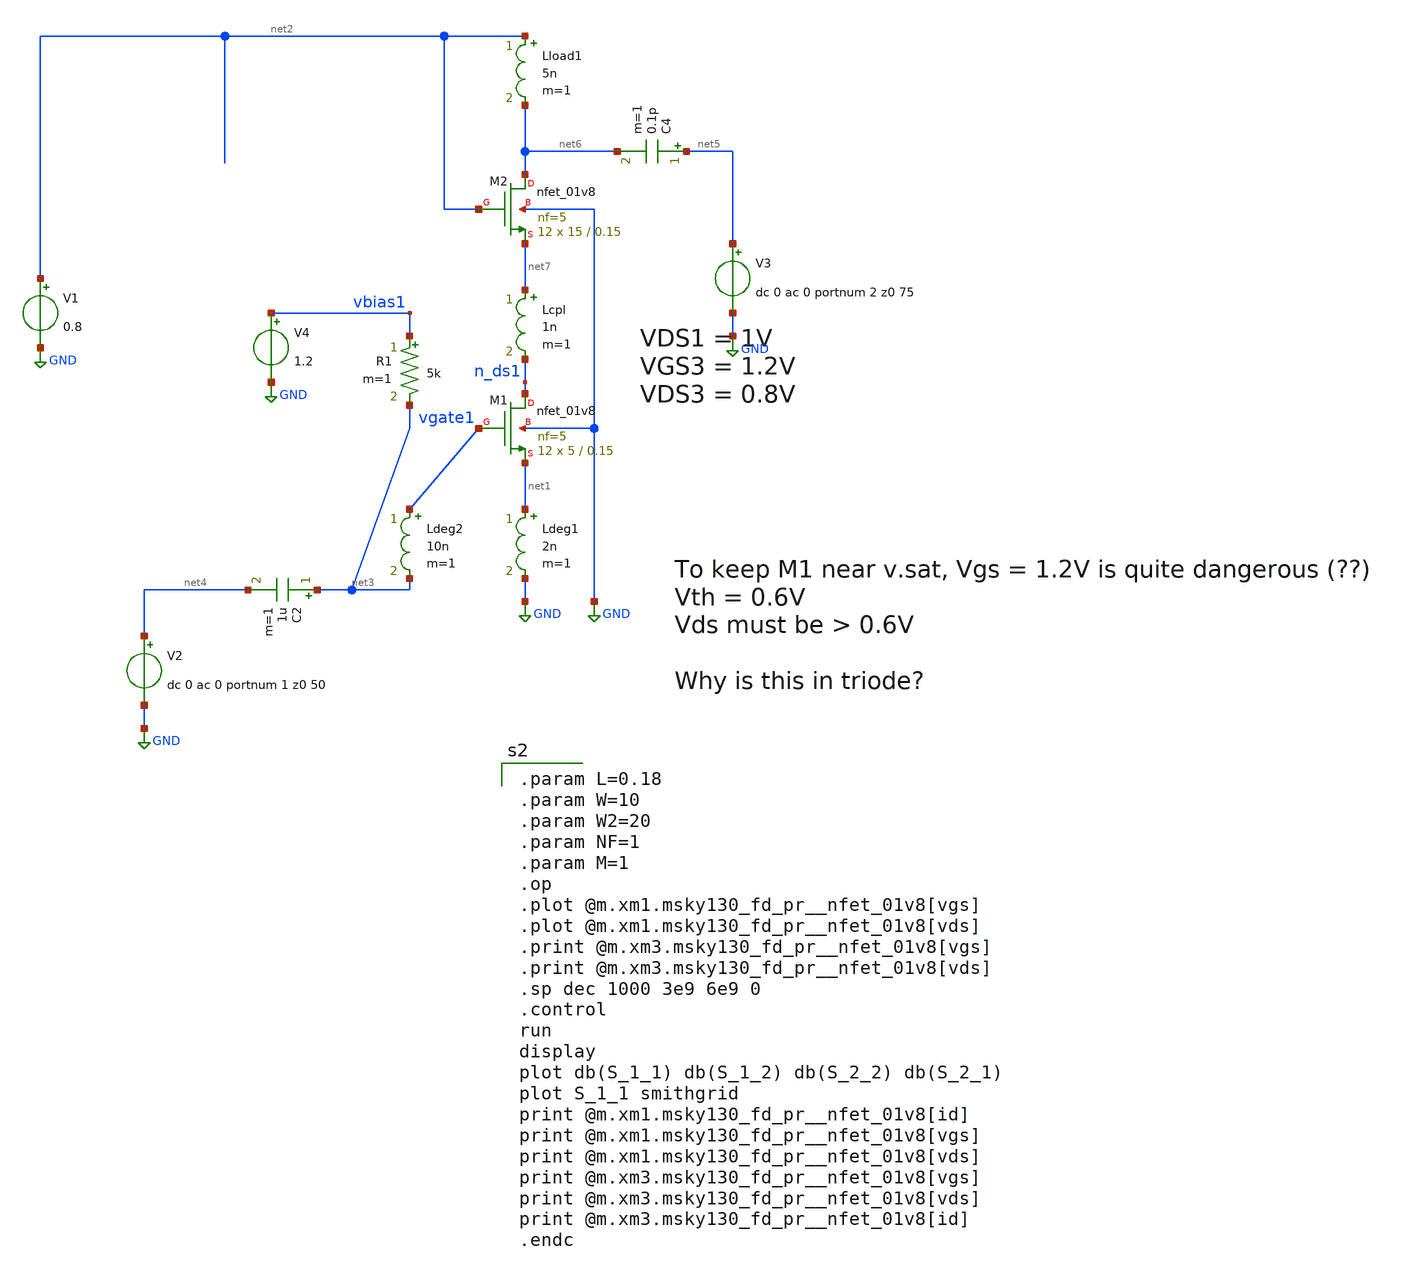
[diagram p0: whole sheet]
** sch_path: xschem/LNA24_1.sch
**.subckt LNA24_1
XM1 n_ds1 vgate1 net1 GND sky130_fd_pr__nfet_01v8 L=0.15 W=5 nf=5 ad='int((nf+1)/2) * W/nf * 0.29' as='int((nf+2)/2) * W/nf * 0.29'
+ pd='2*int((nf+1)/2) * (W/nf + 0.29)' ps='2*int((nf+2)/2) * (W/nf + 0.29)' nrd='0.29 / W' nrs='0.29 / W'
+ sa=0 sb=0 sd=0 mult=12 m=12
Ldeg1 net1 GND 2n m=1
V1 net2 GND 0.8
V2 net4 GND dc 0 ac 0 portnum 1 z0 50
C2 net3 net4 1u m=1
V3 net5 GND dc 0 ac 0 portnum 2 z0 75
C4 net5 net6 0.1p m=1
Ldeg2 vgate1 net3 10n m=1
R1 vbias1 net3 5k m=1
Lload1 net2 net6 5n m=1
V4 vbias1 GND 1.2
XM2 net6 net2 net7 GND sky130_fd_pr__nfet_01v8 L=0.15 W=15 nf=5 ad='int((nf+1)/2) * W/nf * 0.29' as='int((nf+2)/2) * W/nf * 0.29'
+ pd='2*int((nf+1)/2) * (W/nf + 0.29)' ps='2*int((nf+2)/2) * (W/nf + 0.29)' nrd='0.29 / W' nrs='0.29 / W'
+ sa=0 sb=0 sd=0 mult=12 m=12
Lcpl net7 n_ds1 1n m=1
**** begin user architecture code
.lib $::SKYWATER_MODELS/sky130.lib.spice tt
.include $::PDKPATH/libs.ref/sky130_fd_sc_hvl/spice/sky130_fd_sc_hvl.spice

.param L=0.18
.param W=10
.param W2=20
.param NF=1
.param M=1
.op
.plot @m.xm1.msky130_fd_pr__nfet_01v8[vgs]
.plot @m.xm1.msky130_fd_pr__nfet_01v8[vds]
.print @m.xm3.msky130_fd_pr__nfet_01v8[vgs]
.print @m.xm3.msky130_fd_pr__nfet_01v8[vds]
.sp dec 1000 3e9 6e9 0
.control
run
display
plot db(S_1_1) db(S_1_2) db(S_2_2) db(S_2_1)
plot S_1_1 smithgrid
print @m.xm1.msky130_fd_pr__nfet_01v8[id]
print @m.xm1.msky130_fd_pr__nfet_01v8[vgs]
print @m.xm1.msky130_fd_pr__nfet_01v8[vds]
print @m.xm3.msky130_fd_pr__nfet_01v8[vgs]
print @m.xm3.msky130_fd_pr__nfet_01v8[vds]
print @m.xm3.msky130_fd_pr__nfet_01v8[id]
.endc


**** end user architecture code
**.ends
.GLOBAL GND
.end
